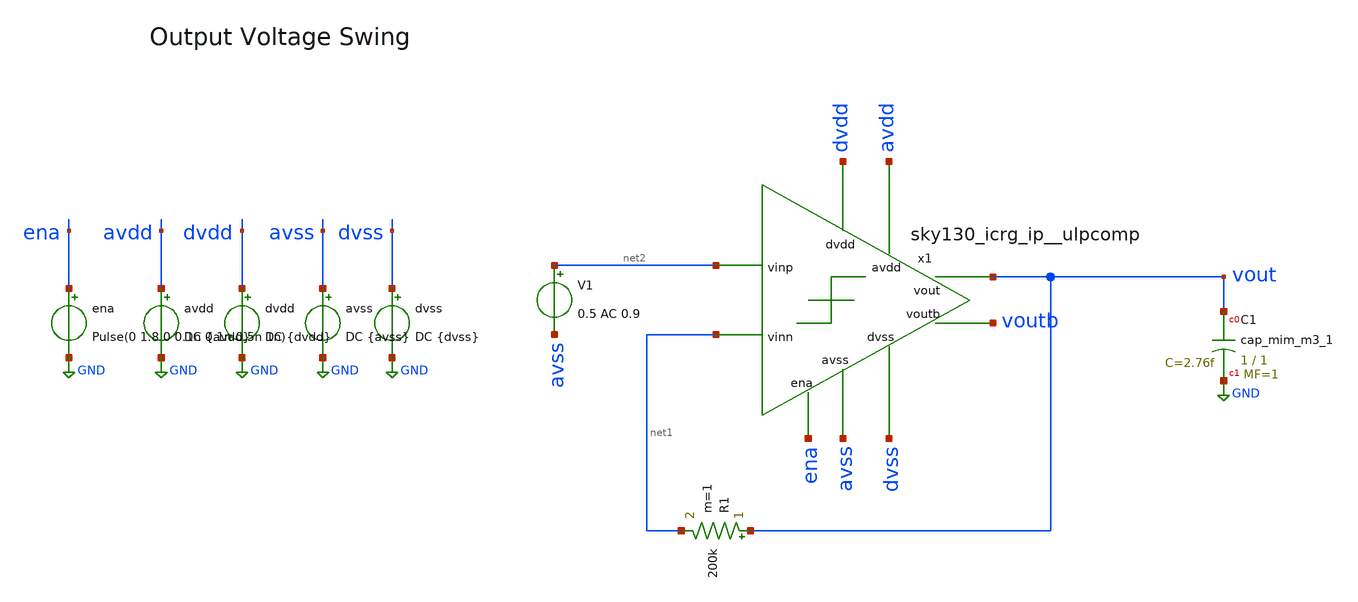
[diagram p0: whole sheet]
** sch_path: cace/tb_voltage_swing.sch
**.subckt tb_voltage_swing
R1 vout net1 200k m=1
x1 dvdd avdd ena net2 net1 vout voutb avss dvss sky130_icrg_ip__ulpcomp
XC1 vout GND sky130_fd_pr__cap_mim_m3_1 W=1 L=1 MF=1 m=1
V1 net2 avss 0.5 AC 0.9
avdd avdd GND DC {avdd}
dvdd dvdd GND DC {dvdd}
avss avss GND DC {avss}
dvss dvss GND DC {dvss}
ena ena GND Pulse(0 1.8 0 0.1n 0.1n 0.5n 1n)
**** begin user architecture code



.include {DUT_path}

.lib /home/ttuser/pdk/sky130A/libs.tech/combined/sky130.lib.spice {corner}

.option TEMP={temperature}

.option warn=1


.control
tran [1.0 / {frequency} / 100] [1 / {frequency}]
set wr_singlescale
wrdata {simpath}/{filename}_{N}.data -V(vout)
quit
.endc

**** end user architecture code
**.ends
.GLOBAL GND
.end
